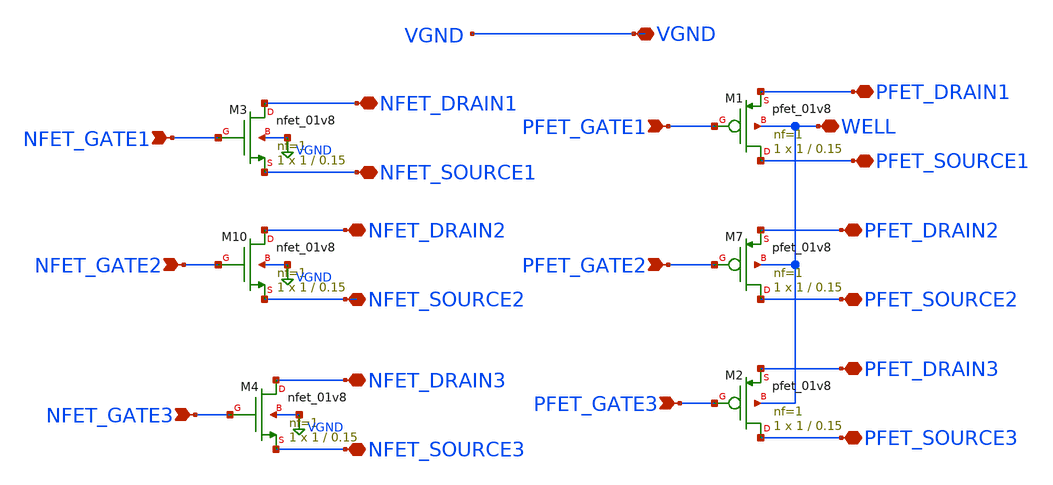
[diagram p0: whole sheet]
** sch_path: libs.ref/sky130_hilas_sc/xschem/sky130_hilas_Trans4small.sch
**.subckt sky130_hilas_Trans4small NFET_GATE2 WELL PFET_SOURCE2 NFET_GATE1 NFET_DRAIN1 PFET_SOURCE3
*+ PFET_GATE3 NFET_DRAIN3 NFET_DRAIN2 PFET_GATE2 PFET_SOURCE1 PFET_GATE1 NFET_GATE3 PFET_DRAIN1 PFET_DRAIN3
*+ PFET_DRAIN2 NFET_SOURCE2 NFET_SOURCE3 NFET_SOURCE1 VGND
*.ipin NFET_GATE2
*.iopin WELL
*.iopin PFET_SOURCE2
*.ipin NFET_GATE1
*.iopin NFET_DRAIN1
*.iopin PFET_SOURCE3
*.ipin PFET_GATE3
*.iopin NFET_DRAIN3
*.iopin NFET_DRAIN2
*.ipin PFET_GATE2
*.iopin PFET_SOURCE1
*.ipin PFET_GATE1
*.ipin NFET_GATE3
*.iopin PFET_DRAIN1
*.iopin PFET_DRAIN3
*.iopin PFET_DRAIN2
*.iopin NFET_SOURCE2
*.iopin NFET_SOURCE3
*.iopin NFET_SOURCE1
*.iopin VGND
XM1 PFET_SOURCE1 PFET_GATE1 PFET_DRAIN1 WELL sky130_fd_pr__pfet_01v8 L=0.15 W=1 nf=1 ad='int((nf+1)/2) * W/nf * 0.29'
+ as='int((nf+2)/2) * W/nf * 0.29' pd='2*int((nf+1)/2) * (W/nf + 0.29)' ps='2*int((nf+2)/2) * (W/nf + 0.29)'
+ nrd='0.29 / W' nrs='0.29 / W' sa=0 sb=0 sd=0 mult=1 m=1
XM2 PFET_SOURCE3 PFET_GATE3 PFET_DRAIN3 WELL sky130_fd_pr__pfet_01v8 L=0.15 W=1 nf=1 ad='int((nf+1)/2) * W/nf * 0.29'
+ as='int((nf+2)/2) * W/nf * 0.29' pd='2*int((nf+1)/2) * (W/nf + 0.29)' ps='2*int((nf+2)/2) * (W/nf + 0.29)'
+ nrd='0.29 / W' nrs='0.29 / W' sa=0 sb=0 sd=0 mult=1 m=1
XM3 NFET_DRAIN1 NFET_GATE1 NFET_SOURCE1 VGND sky130_fd_pr__nfet_01v8 L=0.15 W=1 nf=1 ad='int((nf+1)/2) * W/nf * 0.29'
+ as='int((nf+2)/2) * W/nf * 0.29' pd='2*int((nf+1)/2) * (W/nf + 0.29)' ps='2*int((nf+2)/2) * (W/nf + 0.29)'
+ nrd='0.29 / W' nrs='0.29 / W' sa=0 sb=0 sd=0 mult=1 m=1
XM4 NFET_DRAIN3 NFET_GATE3 NFET_SOURCE3 VGND sky130_fd_pr__nfet_01v8 L=0.15 W=1 nf=1 ad='int((nf+1)/2) * W/nf * 0.29'
+ as='int((nf+2)/2) * W/nf * 0.29' pd='2*int((nf+1)/2) * (W/nf + 0.29)' ps='2*int((nf+2)/2) * (W/nf + 0.29)'
+ nrd='0.29 / W' nrs='0.29 / W' sa=0 sb=0 sd=0 mult=1 m=1
XM7 PFET_SOURCE2 PFET_GATE2 PFET_DRAIN2 WELL sky130_fd_pr__pfet_01v8 L=0.15 W=1 nf=1 ad='int((nf+1)/2) * W/nf * 0.29'
+ as='int((nf+2)/2) * W/nf * 0.29' pd='2*int((nf+1)/2) * (W/nf + 0.29)' ps='2*int((nf+2)/2) * (W/nf + 0.29)'
+ nrd='0.29 / W' nrs='0.29 / W' sa=0 sb=0 sd=0 mult=1 m=1
XM10 NFET_DRAIN2 NFET_GATE2 NFET_SOURCE2 VGND sky130_fd_pr__nfet_01v8 L=0.15 W=1 nf=1 ad='int((nf+1)/2) * W/nf * 0.29'
+ as='int((nf+2)/2) * W/nf * 0.29' pd='2*int((nf+1)/2) * (W/nf + 0.29)' ps='2*int((nf+2)/2) * (W/nf + 0.29)'
+ nrd='0.29 / W' nrs='0.29 / W' sa=0 sb=0 sd=0 mult=1 m=1
**.ends
.GLOBAL VGND
.end
